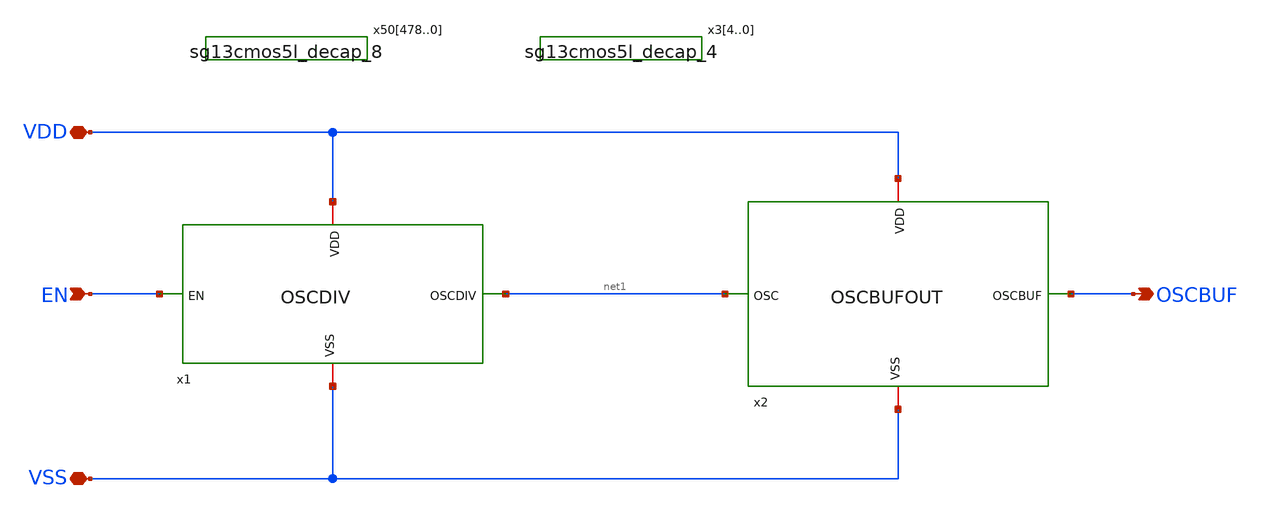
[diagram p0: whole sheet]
** sch_path: MPU9547-main/analog/schematic/ANACORE.sch
**.subckt ANACORE EN VDD VSS OSCBUF
*.ipin EN
*.iopin VDD
*.iopin VSS
*.opin OSCBUF
x1 VDD EN net1 VSS OSCDIV
x2 VDD net1 OSCBUF VSS OSCBUFOUT
x50478 VDD VSS sg13cmos5l_decap_8
x50477 VDD VSS sg13cmos5l_decap_8
x50476 VDD VSS sg13cmos5l_decap_8
x50475 VDD VSS sg13cmos5l_decap_8
x50474 VDD VSS sg13cmos5l_decap_8
x50473 VDD VSS sg13cmos5l_decap_8
x50472 VDD VSS sg13cmos5l_decap_8
x50471 VDD VSS sg13cmos5l_decap_8
x50470 VDD VSS sg13cmos5l_decap_8
x50469 VDD VSS sg13cmos5l_decap_8
x50468 VDD VSS sg13cmos5l_decap_8
x50467 VDD VSS sg13cmos5l_decap_8
x50466 VDD VSS sg13cmos5l_decap_8
x50465 VDD VSS sg13cmos5l_decap_8
x50464 VDD VSS sg13cmos5l_decap_8
x50463 VDD VSS sg13cmos5l_decap_8
x50462 VDD VSS sg13cmos5l_decap_8
x50461 VDD VSS sg13cmos5l_decap_8
x50460 VDD VSS sg13cmos5l_decap_8
x50459 VDD VSS sg13cmos5l_decap_8
x50458 VDD VSS sg13cmos5l_decap_8
x50457 VDD VSS sg13cmos5l_decap_8
x50456 VDD VSS sg13cmos5l_decap_8
x50455 VDD VSS sg13cmos5l_decap_8
x50454 VDD VSS sg13cmos5l_decap_8
x50453 VDD VSS sg13cmos5l_decap_8
x50452 VDD VSS sg13cmos5l_decap_8
x50451 VDD VSS sg13cmos5l_decap_8
x50450 VDD VSS sg13cmos5l_decap_8
x50449 VDD VSS sg13cmos5l_decap_8
x50448 VDD VSS sg13cmos5l_decap_8
x50447 VDD VSS sg13cmos5l_decap_8
x50446 VDD VSS sg13cmos5l_decap_8
x50445 VDD VSS sg13cmos5l_decap_8
x50444 VDD VSS sg13cmos5l_decap_8
x50443 VDD VSS sg13cmos5l_decap_8
x50442 VDD VSS sg13cmos5l_decap_8
x50441 VDD VSS sg13cmos5l_decap_8
x50440 VDD VSS sg13cmos5l_decap_8
x50439 VDD VSS sg13cmos5l_decap_8
x50438 VDD VSS sg13cmos5l_decap_8
x50437 VDD VSS sg13cmos5l_decap_8
x50436 VDD VSS sg13cmos5l_decap_8
x50435 VDD VSS sg13cmos5l_decap_8
x50434 VDD VSS sg13cmos5l_decap_8
x50433 VDD VSS sg13cmos5l_decap_8
x50432 VDD VSS sg13cmos5l_decap_8
x50431 VDD VSS sg13cmos5l_decap_8
x50430 VDD VSS sg13cmos5l_decap_8
x50429 VDD VSS sg13cmos5l_decap_8
x50428 VDD VSS sg13cmos5l_decap_8
x50427 VDD VSS sg13cmos5l_decap_8
x50426 VDD VSS sg13cmos5l_decap_8
x50425 VDD VSS sg13cmos5l_decap_8
x50424 VDD VSS sg13cmos5l_decap_8
x50423 VDD VSS sg13cmos5l_decap_8
x50422 VDD VSS sg13cmos5l_decap_8
x50421 VDD VSS sg13cmos5l_decap_8
x50420 VDD VSS sg13cmos5l_decap_8
x50419 VDD VSS sg13cmos5l_decap_8
x50418 VDD VSS sg13cmos5l_decap_8
x50417 VDD VSS sg13cmos5l_decap_8
x50416 VDD VSS sg13cmos5l_decap_8
x50415 VDD VSS sg13cmos5l_decap_8
x50414 VDD VSS sg13cmos5l_decap_8
x50413 VDD VSS sg13cmos5l_decap_8
x50412 VDD VSS sg13cmos5l_decap_8
x50411 VDD VSS sg13cmos5l_decap_8
x50410 VDD VSS sg13cmos5l_decap_8
x50409 VDD VSS sg13cmos5l_decap_8
x50408 VDD VSS sg13cmos5l_decap_8
x50407 VDD VSS sg13cmos5l_decap_8
x50406 VDD VSS sg13cmos5l_decap_8
x50405 VDD VSS sg13cmos5l_decap_8
x50404 VDD VSS sg13cmos5l_decap_8
x50403 VDD VSS sg13cmos5l_decap_8
x50402 VDD VSS sg13cmos5l_decap_8
x50401 VDD VSS sg13cmos5l_decap_8
x50400 VDD VSS sg13cmos5l_decap_8
x50399 VDD VSS sg13cmos5l_decap_8
x50398 VDD VSS sg13cmos5l_decap_8
x50397 VDD VSS sg13cmos5l_decap_8
x50396 VDD VSS sg13cmos5l_decap_8
x50395 VDD VSS sg13cmos5l_decap_8
x50394 VDD VSS sg13cmos5l_decap_8
x50393 VDD VSS sg13cmos5l_decap_8
x50392 VDD VSS sg13cmos5l_decap_8
x50391 VDD VSS sg13cmos5l_decap_8
x50390 VDD VSS sg13cmos5l_decap_8
x50389 VDD VSS sg13cmos5l_decap_8
x50388 VDD VSS sg13cmos5l_decap_8
x50387 VDD VSS sg13cmos5l_decap_8
x50386 VDD VSS sg13cmos5l_decap_8
x50385 VDD VSS sg13cmos5l_decap_8
x50384 VDD VSS sg13cmos5l_decap_8
x50383 VDD VSS sg13cmos5l_decap_8
x50382 VDD VSS sg13cmos5l_decap_8
x50381 VDD VSS sg13cmos5l_decap_8
x50380 VDD VSS sg13cmos5l_decap_8
x50379 VDD VSS sg13cmos5l_decap_8
x50378 VDD VSS sg13cmos5l_decap_8
x50377 VDD VSS sg13cmos5l_decap_8
x50376 VDD VSS sg13cmos5l_decap_8
x50375 VDD VSS sg13cmos5l_decap_8
x50374 VDD VSS sg13cmos5l_decap_8
x50373 VDD VSS sg13cmos5l_decap_8
x50372 VDD VSS sg13cmos5l_decap_8
x50371 VDD VSS sg13cmos5l_decap_8
x50370 VDD VSS sg13cmos5l_decap_8
x50369 VDD VSS sg13cmos5l_decap_8
x50368 VDD VSS sg13cmos5l_decap_8
x50367 VDD VSS sg13cmos5l_decap_8
x50366 VDD VSS sg13cmos5l_decap_8
x50365 VDD VSS sg13cmos5l_decap_8
x50364 VDD VSS sg13cmos5l_decap_8
x50363 VDD VSS sg13cmos5l_decap_8
x50362 VDD VSS sg13cmos5l_decap_8
x50361 VDD VSS sg13cmos5l_decap_8
x50360 VDD VSS sg13cmos5l_decap_8
x50359 VDD VSS sg13cmos5l_decap_8
x50358 VDD VSS sg13cmos5l_decap_8
x50357 VDD VSS sg13cmos5l_decap_8
x50356 VDD VSS sg13cmos5l_decap_8
x50355 VDD VSS sg13cmos5l_decap_8
x50354 VDD VSS sg13cmos5l_decap_8
x50353 VDD VSS sg13cmos5l_decap_8
x50352 VDD VSS sg13cmos5l_decap_8
x50351 VDD VSS sg13cmos5l_decap_8
x50350 VDD VSS sg13cmos5l_decap_8
x50349 VDD VSS sg13cmos5l_decap_8
x50348 VDD VSS sg13cmos5l_decap_8
x50347 VDD VSS sg13cmos5l_decap_8
x50346 VDD VSS sg13cmos5l_decap_8
x50345 VDD VSS sg13cmos5l_decap_8
x50344 VDD VSS sg13cmos5l_decap_8
x50343 VDD VSS sg13cmos5l_decap_8
x50342 VDD VSS sg13cmos5l_decap_8
x50341 VDD VSS sg13cmos5l_decap_8
x50340 VDD VSS sg13cmos5l_decap_8
x50339 VDD VSS sg13cmos5l_decap_8
x50338 VDD VSS sg13cmos5l_decap_8
x50337 VDD VSS sg13cmos5l_decap_8
x50336 VDD VSS sg13cmos5l_decap_8
x50335 VDD VSS sg13cmos5l_decap_8
x50334 VDD VSS sg13cmos5l_decap_8
x50333 VDD VSS sg13cmos5l_decap_8
x50332 VDD VSS sg13cmos5l_decap_8
x50331 VDD VSS sg13cmos5l_decap_8
x50330 VDD VSS sg13cmos5l_decap_8
x50329 VDD VSS sg13cmos5l_decap_8
x50328 VDD VSS sg13cmos5l_decap_8
x50327 VDD VSS sg13cmos5l_decap_8
x50326 VDD VSS sg13cmos5l_decap_8
x50325 VDD VSS sg13cmos5l_decap_8
x50324 VDD VSS sg13cmos5l_decap_8
x50323 VDD VSS sg13cmos5l_decap_8
x50322 VDD VSS sg13cmos5l_decap_8
x50321 VDD VSS sg13cmos5l_decap_8
x50320 VDD VSS sg13cmos5l_decap_8
x50319 VDD VSS sg13cmos5l_decap_8
x50318 VDD VSS sg13cmos5l_decap_8
x50317 VDD VSS sg13cmos5l_decap_8
x50316 VDD VSS sg13cmos5l_decap_8
x50315 VDD VSS sg13cmos5l_decap_8
x50314 VDD VSS sg13cmos5l_decap_8
x50313 VDD VSS sg13cmos5l_decap_8
x50312 VDD VSS sg13cmos5l_decap_8
x50311 VDD VSS sg13cmos5l_decap_8
x50310 VDD VSS sg13cmos5l_decap_8
x50309 VDD VSS sg13cmos5l_decap_8
x50308 VDD VSS sg13cmos5l_decap_8
x50307 VDD VSS sg13cmos5l_decap_8
x50306 VDD VSS sg13cmos5l_decap_8
x50305 VDD VSS sg13cmos5l_decap_8
x50304 VDD VSS sg13cmos5l_decap_8
x50303 VDD VSS sg13cmos5l_decap_8
x50302 VDD VSS sg13cmos5l_decap_8
x50301 VDD VSS sg13cmos5l_decap_8
x50300 VDD VSS sg13cmos5l_decap_8
x50299 VDD VSS sg13cmos5l_decap_8
x50298 VDD VSS sg13cmos5l_decap_8
x50297 VDD VSS sg13cmos5l_decap_8
x50296 VDD VSS sg13cmos5l_decap_8
x50295 VDD VSS sg13cmos5l_decap_8
x50294 VDD VSS sg13cmos5l_decap_8
x50293 VDD VSS sg13cmos5l_decap_8
x50292 VDD VSS sg13cmos5l_decap_8
x50291 VDD VSS sg13cmos5l_decap_8
x50290 VDD VSS sg13cmos5l_decap_8
x50289 VDD VSS sg13cmos5l_decap_8
x50288 VDD VSS sg13cmos5l_decap_8
x50287 VDD VSS sg13cmos5l_decap_8
x50286 VDD VSS sg13cmos5l_decap_8
x50285 VDD VSS sg13cmos5l_decap_8
x50284 VDD VSS sg13cmos5l_decap_8
x50283 VDD VSS sg13cmos5l_decap_8
x50282 VDD VSS sg13cmos5l_decap_8
x50281 VDD VSS sg13cmos5l_decap_8
x50280 VDD VSS sg13cmos5l_decap_8
x50279 VDD VSS sg13cmos5l_decap_8
x50278 VDD VSS sg13cmos5l_decap_8
x50277 VDD VSS sg13cmos5l_decap_8
x50276 VDD VSS sg13cmos5l_decap_8
x50275 VDD VSS sg13cmos5l_decap_8
x50274 VDD VSS sg13cmos5l_decap_8
x50273 VDD VSS sg13cmos5l_decap_8
x50272 VDD VSS sg13cmos5l_decap_8
x50271 VDD VSS sg13cmos5l_decap_8
x50270 VDD VSS sg13cmos5l_decap_8
x50269 VDD VSS sg13cmos5l_decap_8
x50268 VDD VSS sg13cmos5l_decap_8
x50267 VDD VSS sg13cmos5l_decap_8
x50266 VDD VSS sg13cmos5l_decap_8
x50265 VDD VSS sg13cmos5l_decap_8
x50264 VDD VSS sg13cmos5l_decap_8
x50263 VDD VSS sg13cmos5l_decap_8
x50262 VDD VSS sg13cmos5l_decap_8
x50261 VDD VSS sg13cmos5l_decap_8
x50260 VDD VSS sg13cmos5l_decap_8
x50259 VDD VSS sg13cmos5l_decap_8
x50258 VDD VSS sg13cmos5l_decap_8
x50257 VDD VSS sg13cmos5l_decap_8
x50256 VDD VSS sg13cmos5l_decap_8
x50255 VDD VSS sg13cmos5l_decap_8
x50254 VDD VSS sg13cmos5l_decap_8
x50253 VDD VSS sg13cmos5l_decap_8
x50252 VDD VSS sg13cmos5l_decap_8
x50251 VDD VSS sg13cmos5l_decap_8
x50250 VDD VSS sg13cmos5l_decap_8
x50249 VDD VSS sg13cmos5l_decap_8
x50248 VDD VSS sg13cmos5l_decap_8
x50247 VDD VSS sg13cmos5l_decap_8
x50246 VDD VSS sg13cmos5l_decap_8
x50245 VDD VSS sg13cmos5l_decap_8
x50244 VDD VSS sg13cmos5l_decap_8
x50243 VDD VSS sg13cmos5l_decap_8
x50242 VDD VSS sg13cmos5l_decap_8
x50241 VDD VSS sg13cmos5l_decap_8
x50240 VDD VSS sg13cmos5l_decap_8
x50239 VDD VSS sg13cmos5l_decap_8
x50238 VDD VSS sg13cmos5l_decap_8
x50237 VDD VSS sg13cmos5l_decap_8
x50236 VDD VSS sg13cmos5l_decap_8
x50235 VDD VSS sg13cmos5l_decap_8
x50234 VDD VSS sg13cmos5l_decap_8
x50233 VDD VSS sg13cmos5l_decap_8
x50232 VDD VSS sg13cmos5l_decap_8
x50231 VDD VSS sg13cmos5l_decap_8
x50230 VDD VSS sg13cmos5l_decap_8
x50229 VDD VSS sg13cmos5l_decap_8
x50228 VDD VSS sg13cmos5l_decap_8
x50227 VDD VSS sg13cmos5l_decap_8
x50226 VDD VSS sg13cmos5l_decap_8
x50225 VDD VSS sg13cmos5l_decap_8
x50224 VDD VSS sg13cmos5l_decap_8
x50223 VDD VSS sg13cmos5l_decap_8
x50222 VDD VSS sg13cmos5l_decap_8
x50221 VDD VSS sg13cmos5l_decap_8
x50220 VDD VSS sg13cmos5l_decap_8
x50219 VDD VSS sg13cmos5l_decap_8
x50218 VDD VSS sg13cmos5l_decap_8
x50217 VDD VSS sg13cmos5l_decap_8
x50216 VDD VSS sg13cmos5l_decap_8
x50215 VDD VSS sg13cmos5l_decap_8
x50214 VDD VSS sg13cmos5l_decap_8
x50213 VDD VSS sg13cmos5l_decap_8
x50212 VDD VSS sg13cmos5l_decap_8
x50211 VDD VSS sg13cmos5l_decap_8
x50210 VDD VSS sg13cmos5l_decap_8
x50209 VDD VSS sg13cmos5l_decap_8
x50208 VDD VSS sg13cmos5l_decap_8
x50207 VDD VSS sg13cmos5l_decap_8
x50206 VDD VSS sg13cmos5l_decap_8
x50205 VDD VSS sg13cmos5l_decap_8
x50204 VDD VSS sg13cmos5l_decap_8
x50203 VDD VSS sg13cmos5l_decap_8
x50202 VDD VSS sg13cmos5l_decap_8
x50201 VDD VSS sg13cmos5l_decap_8
x50200 VDD VSS sg13cmos5l_decap_8
x50199 VDD VSS sg13cmos5l_decap_8
x50198 VDD VSS sg13cmos5l_decap_8
x50197 VDD VSS sg13cmos5l_decap_8
x50196 VDD VSS sg13cmos5l_decap_8
x50195 VDD VSS sg13cmos5l_decap_8
x50194 VDD VSS sg13cmos5l_decap_8
x50193 VDD VSS sg13cmos5l_decap_8
x50192 VDD VSS sg13cmos5l_decap_8
x50191 VDD VSS sg13cmos5l_decap_8
x50190 VDD VSS sg13cmos5l_decap_8
x50189 VDD VSS sg13cmos5l_decap_8
x50188 VDD VSS sg13cmos5l_decap_8
x50187 VDD VSS sg13cmos5l_decap_8
x50186 VDD VSS sg13cmos5l_decap_8
x50185 VDD VSS sg13cmos5l_decap_8
x50184 VDD VSS sg13cmos5l_decap_8
x50183 VDD VSS sg13cmos5l_decap_8
x50182 VDD VSS sg13cmos5l_decap_8
x50181 VDD VSS sg13cmos5l_decap_8
x50180 VDD VSS sg13cmos5l_decap_8
x50179 VDD VSS sg13cmos5l_decap_8
x50178 VDD VSS sg13cmos5l_decap_8
x50177 VDD VSS sg13cmos5l_decap_8
x50176 VDD VSS sg13cmos5l_decap_8
x50175 VDD VSS sg13cmos5l_decap_8
x50174 VDD VSS sg13cmos5l_decap_8
x50173 VDD VSS sg13cmos5l_decap_8
x50172 VDD VSS sg13cmos5l_decap_8
x50171 VDD VSS sg13cmos5l_decap_8
x50170 VDD VSS sg13cmos5l_decap_8
x50169 VDD VSS sg13cmos5l_decap_8
x50168 VDD VSS sg13cmos5l_decap_8
x50167 VDD VSS sg13cmos5l_decap_8
x50166 VDD VSS sg13cmos5l_decap_8
x50165 VDD VSS sg13cmos5l_decap_8
x50164 VDD VSS sg13cmos5l_decap_8
x50163 VDD VSS sg13cmos5l_decap_8
x50162 VDD VSS sg13cmos5l_decap_8
x50161 VDD VSS sg13cmos5l_decap_8
x50160 VDD VSS sg13cmos5l_decap_8
x50159 VDD VSS sg13cmos5l_decap_8
x50158 VDD VSS sg13cmos5l_decap_8
x50157 VDD VSS sg13cmos5l_decap_8
x50156 VDD VSS sg13cmos5l_decap_8
x50155 VDD VSS sg13cmos5l_decap_8
x50154 VDD VSS sg13cmos5l_decap_8
x50153 VDD VSS sg13cmos5l_decap_8
x50152 VDD VSS sg13cmos5l_decap_8
x50151 VDD VSS sg13cmos5l_decap_8
x50150 VDD VSS sg13cmos5l_decap_8
x50149 VDD VSS sg13cmos5l_decap_8
x50148 VDD VSS sg13cmos5l_decap_8
x50147 VDD VSS sg13cmos5l_decap_8
x50146 VDD VSS sg13cmos5l_decap_8
x50145 VDD VSS sg13cmos5l_decap_8
x50144 VDD VSS sg13cmos5l_decap_8
x50143 VDD VSS sg13cmos5l_decap_8
x50142 VDD VSS sg13cmos5l_decap_8
x50141 VDD VSS sg13cmos5l_decap_8
x50140 VDD VSS sg13cmos5l_decap_8
x50139 VDD VSS sg13cmos5l_decap_8
x50138 VDD VSS sg13cmos5l_decap_8
x50137 VDD VSS sg13cmos5l_decap_8
x50136 VDD VSS sg13cmos5l_decap_8
x50135 VDD VSS sg13cmos5l_decap_8
x50134 VDD VSS sg13cmos5l_decap_8
x50133 VDD VSS sg13cmos5l_decap_8
x50132 VDD VSS sg13cmos5l_decap_8
x50131 VDD VSS sg13cmos5l_decap_8
x50130 VDD VSS sg13cmos5l_decap_8
x50129 VDD VSS sg13cmos5l_decap_8
x50128 VDD VSS sg13cmos5l_decap_8
x50127 VDD VSS sg13cmos5l_decap_8
x50126 VDD VSS sg13cmos5l_decap_8
x50125 VDD VSS sg13cmos5l_decap_8
x50124 VDD VSS sg13cmos5l_decap_8
x50123 VDD VSS sg13cmos5l_decap_8
x50122 VDD VSS sg13cmos5l_decap_8
x50121 VDD VSS sg13cmos5l_decap_8
x50120 VDD VSS sg13cmos5l_decap_8
x50119 VDD VSS sg13cmos5l_decap_8
x50118 VDD VSS sg13cmos5l_decap_8
x50117 VDD VSS sg13cmos5l_decap_8
x50116 VDD VSS sg13cmos5l_decap_8
x50115 VDD VSS sg13cmos5l_decap_8
x50114 VDD VSS sg13cmos5l_decap_8
x50113 VDD VSS sg13cmos5l_decap_8
x50112 VDD VSS sg13cmos5l_decap_8
x50111 VDD VSS sg13cmos5l_decap_8
x50110 VDD VSS sg13cmos5l_decap_8
x50109 VDD VSS sg13cmos5l_decap_8
x50108 VDD VSS sg13cmos5l_decap_8
x50107 VDD VSS sg13cmos5l_decap_8
x50106 VDD VSS sg13cmos5l_decap_8
x50105 VDD VSS sg13cmos5l_decap_8
x50104 VDD VSS sg13cmos5l_decap_8
x50103 VDD VSS sg13cmos5l_decap_8
x50102 VDD VSS sg13cmos5l_decap_8
x50101 VDD VSS sg13cmos5l_decap_8
x50100 VDD VSS sg13cmos5l_decap_8
x5099 VDD VSS sg13cmos5l_decap_8
x5098 VDD VSS sg13cmos5l_decap_8
x5097 VDD VSS sg13cmos5l_decap_8
x5096 VDD VSS sg13cmos5l_decap_8
x5095 VDD VSS sg13cmos5l_decap_8
x5094 VDD VSS sg13cmos5l_decap_8
x5093 VDD VSS sg13cmos5l_decap_8
x5092 VDD VSS sg13cmos5l_decap_8
x5091 VDD VSS sg13cmos5l_decap_8
x5090 VDD VSS sg13cmos5l_decap_8
x5089 VDD VSS sg13cmos5l_decap_8
x5088 VDD VSS sg13cmos5l_decap_8
x5087 VDD VSS sg13cmos5l_decap_8
x5086 VDD VSS sg13cmos5l_decap_8
x5085 VDD VSS sg13cmos5l_decap_8
x5084 VDD VSS sg13cmos5l_decap_8
x5083 VDD VSS sg13cmos5l_decap_8
x5082 VDD VSS sg13cmos5l_decap_8
x5081 VDD VSS sg13cmos5l_decap_8
x5080 VDD VSS sg13cmos5l_decap_8
x5079 VDD VSS sg13cmos5l_decap_8
x5078 VDD VSS sg13cmos5l_decap_8
x5077 VDD VSS sg13cmos5l_decap_8
x5076 VDD VSS sg13cmos5l_decap_8
x5075 VDD VSS sg13cmos5l_decap_8
x5074 VDD VSS sg13cmos5l_decap_8
x5073 VDD VSS sg13cmos5l_decap_8
x5072 VDD VSS sg13cmos5l_decap_8
x5071 VDD VSS sg13cmos5l_decap_8
x5070 VDD VSS sg13cmos5l_decap_8
x5069 VDD VSS sg13cmos5l_decap_8
x5068 VDD VSS sg13cmos5l_decap_8
x5067 VDD VSS sg13cmos5l_decap_8
x5066 VDD VSS sg13cmos5l_decap_8
x5065 VDD VSS sg13cmos5l_decap_8
x5064 VDD VSS sg13cmos5l_decap_8
x5063 VDD VSS sg13cmos5l_decap_8
x5062 VDD VSS sg13cmos5l_decap_8
x5061 VDD VSS sg13cmos5l_decap_8
x5060 VDD VSS sg13cmos5l_decap_8
x5059 VDD VSS sg13cmos5l_decap_8
x5058 VDD VSS sg13cmos5l_decap_8
x5057 VDD VSS sg13cmos5l_decap_8
x5056 VDD VSS sg13cmos5l_decap_8
x5055 VDD VSS sg13cmos5l_decap_8
x5054 VDD VSS sg13cmos5l_decap_8
x5053 VDD VSS sg13cmos5l_decap_8
x5052 VDD VSS sg13cmos5l_decap_8
x5051 VDD VSS sg13cmos5l_decap_8
x5050 VDD VSS sg13cmos5l_decap_8
x5049 VDD VSS sg13cmos5l_decap_8
x5048 VDD VSS sg13cmos5l_decap_8
x5047 VDD VSS sg13cmos5l_decap_8
x5046 VDD VSS sg13cmos5l_decap_8
x5045 VDD VSS sg13cmos5l_decap_8
x5044 VDD VSS sg13cmos5l_decap_8
x5043 VDD VSS sg13cmos5l_decap_8
x5042 VDD VSS sg13cmos5l_decap_8
x5041 VDD VSS sg13cmos5l_decap_8
x5040 VDD VSS sg13cmos5l_decap_8
x5039 VDD VSS sg13cmos5l_decap_8
x5038 VDD VSS sg13cmos5l_decap_8
x5037 VDD VSS sg13cmos5l_decap_8
x5036 VDD VSS sg13cmos5l_decap_8
x5035 VDD VSS sg13cmos5l_decap_8
x5034 VDD VSS sg13cmos5l_decap_8
x5033 VDD VSS sg13cmos5l_decap_8
x5032 VDD VSS sg13cmos5l_decap_8
x5031 VDD VSS sg13cmos5l_decap_8
x5030 VDD VSS sg13cmos5l_decap_8
x5029 VDD VSS sg13cmos5l_decap_8
x5028 VDD VSS sg13cmos5l_decap_8
x5027 VDD VSS sg13cmos5l_decap_8
x5026 VDD VSS sg13cmos5l_decap_8
x5025 VDD VSS sg13cmos5l_decap_8
x5024 VDD VSS sg13cmos5l_decap_8
x5023 VDD VSS sg13cmos5l_decap_8
x5022 VDD VSS sg13cmos5l_decap_8
x5021 VDD VSS sg13cmos5l_decap_8
x5020 VDD VSS sg13cmos5l_decap_8
x5019 VDD VSS sg13cmos5l_decap_8
x5018 VDD VSS sg13cmos5l_decap_8
x5017 VDD VSS sg13cmos5l_decap_8
x5016 VDD VSS sg13cmos5l_decap_8
x5015 VDD VSS sg13cmos5l_decap_8
x5014 VDD VSS sg13cmos5l_decap_8
x5013 VDD VSS sg13cmos5l_decap_8
x5012 VDD VSS sg13cmos5l_decap_8
x5011 VDD VSS sg13cmos5l_decap_8
x5010 VDD VSS sg13cmos5l_decap_8
x509 VDD VSS sg13cmos5l_decap_8
x508 VDD VSS sg13cmos5l_decap_8
x507 VDD VSS sg13cmos5l_decap_8
x506 VDD VSS sg13cmos5l_decap_8
x505 VDD VSS sg13cmos5l_decap_8
x504 VDD VSS sg13cmos5l_decap_8
x503 VDD VSS sg13cmos5l_decap_8
x502 VDD VSS sg13cmos5l_decap_8
x501 VDD VSS sg13cmos5l_decap_8
x500 VDD VSS sg13cmos5l_decap_8
x34 VDD VSS sg13cmos5l_decap_4
x33 VDD VSS sg13cmos5l_decap_4
x32 VDD VSS sg13cmos5l_decap_4
x31 VDD VSS sg13cmos5l_decap_4
x30 VDD VSS sg13cmos5l_decap_4
**.ends
.end
